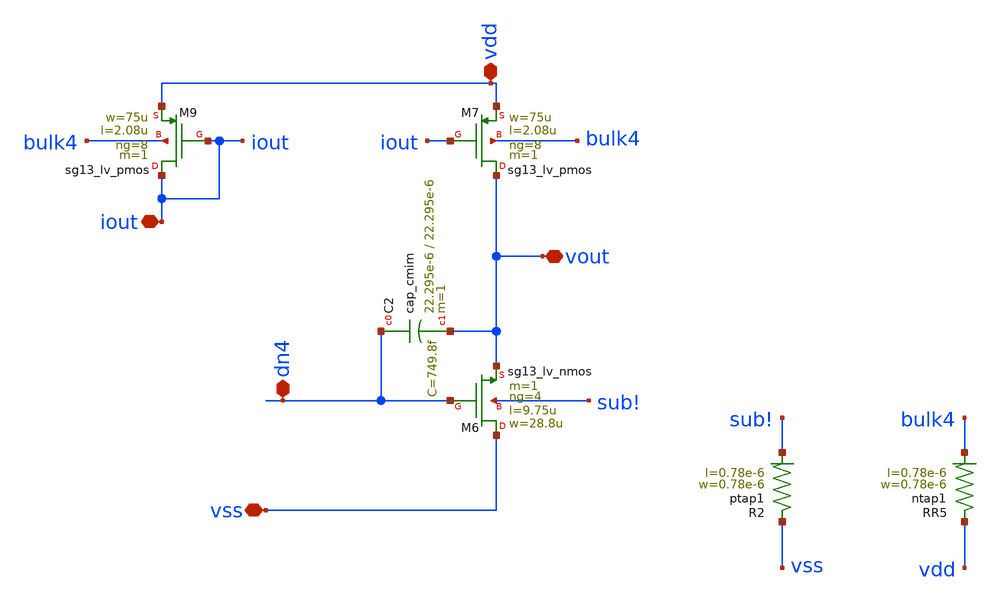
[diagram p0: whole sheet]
** sch_path: schematic/bgr/part_3_layout/OTA_layout/output_stage/schematic_mod/output_stage.sch
**.subckt output_stage vdd iout vout vss dn4
*.iopin vdd
*.iopin iout
*.iopin vout
*.iopin vss
*.iopin dn4
XM7 vout iout vdd bulk4 sg13_lv_pmos w=75u l=2.08u ng=8 m=1 mm_ok=1
XM6 vss dn4 vout sub! sg13_lv_nmos w=28.8u l=9.75u ng=4 m=1 mm_ok=1
XM9 iout iout vdd bulk4 sg13_lv_pmos w=75u l=2.08u ng=8 m=1 mm_ok=1
XC2 dn4 vout cap_cmim w=22.295e-6 l=22.295e-6 m=1 mm_ok=1
XR2 vss sub! ptap1 R=262.8 w=0.78e-6 l=0.78e-6
XR5 vdd bulk4 ntap1 R=262.8 w=0.78e-6 l=0.78e-6
**.ends
.end
